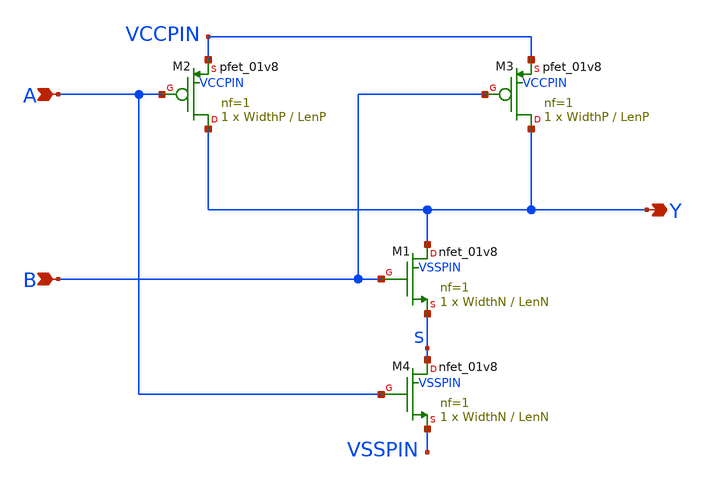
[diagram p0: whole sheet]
** sch_path: sky130_tests/lvnand.sch
* Copyright 2021 Stefan Frederik Schippers
* Licensed under the Apache License, Version 2.0 (the "License");
* you may not use this file except in compliance with the License.
* You may obtain a copy of the License at
* https://www.apache.org/licenses/LICENSE-2.0
* Unless required by applicable law or agreed to in writing, software
* distributed under the License is distributed on an "AS IS" BASIS,
* WITHOUT WARRANTIES OR CONDITIONS OF ANY KIND, either express or implied.
* See the License for the specific language governing permissions and
* limitations under the License.
**.subckt lvnand A B Y
*.ipin A
*.ipin B
*.opin Y
XM1 Y B S VSSPIN sky130_fd_pr__nfet_01v8 L=LenN W=WidthN nf=1 ad='int((nf+1)/2) * W/nf * 0.29' as='int((nf+2)/2) * W/nf * 0.29'
+ pd='2*int((nf+1)/2) * (W/nf + 0.29)' ps='2*int((nf+2)/2) * (W/nf + 0.29)' nrd='0.29 / W' nrs='0.29 / W'
+ sa=0 sb=0 sd=0 mult=1 m=1
XM2 Y A VCCPIN VCCPIN sky130_fd_pr__pfet_01v8 L=LenP W=WidthP nf=1 ad='int((nf+1)/2) * W/nf * 0.29' as='int((nf+2)/2) * W/nf * 0.29'
+ pd='2*int((nf+1)/2) * (W/nf + 0.29)' ps='2*int((nf+2)/2) * (W/nf + 0.29)' nrd='0.29 / W' nrs='0.29 / W'
+ sa=0 sb=0 sd=0 mult=1 m=1
XM3 Y B VCCPIN VCCPIN sky130_fd_pr__pfet_01v8 L=LenP W=WidthP nf=1 ad='int((nf+1)/2) * W/nf * 0.29' as='int((nf+2)/2) * W/nf * 0.29'
+ pd='2*int((nf+1)/2) * (W/nf + 0.29)' ps='2*int((nf+2)/2) * (W/nf + 0.29)' nrd='0.29 / W' nrs='0.29 / W'
+ sa=0 sb=0 sd=0 mult=1 m=1
XM4 S A VSSPIN VSSPIN sky130_fd_pr__nfet_01v8 L=LenN W=WidthN nf=1 ad='int((nf+1)/2) * W/nf * 0.29' as='int((nf+2)/2) * W/nf * 0.29'
+ pd='2*int((nf+1)/2) * (W/nf + 0.29)' ps='2*int((nf+2)/2) * (W/nf + 0.29)' nrd='0.29 / W' nrs='0.29 / W'
+ sa=0 sb=0 sd=0 mult=1 m=1
**** begin user architecture code
 ** manual skywater pdks install (with patches applied)
* .lib $::SKYWATER_MODELS/models/sky130.lib.spice tt_mm

** opencircuitdesign pdks install
.lib $::SKYWATER_MODELS/sky130.lib.spice tt_mm


**** end user architecture code
**.ends
**** begin user architecture code

* .option SCALE=1e-6
.option method=gear seed=12
.param L=0.15
.param W=0.5

vd d 0 0
vg g 0 0
.control
dc vd 0 2 0.01 vg 0 2 0.2
alterparam L=0.18
alterparam W=1
reset
dc vd 0 2 0.01 vg 0 2 0.2
alterparam L=0.3
alterparam W=2
reset
dc vd 0 2 0.01 vg 0 2 0.2
alterparam L=0.5
alterparam W=3
reset
dc vd 0 2 0.01 vg 0 2 0.2

.endc





**** end user architecture code
.end
